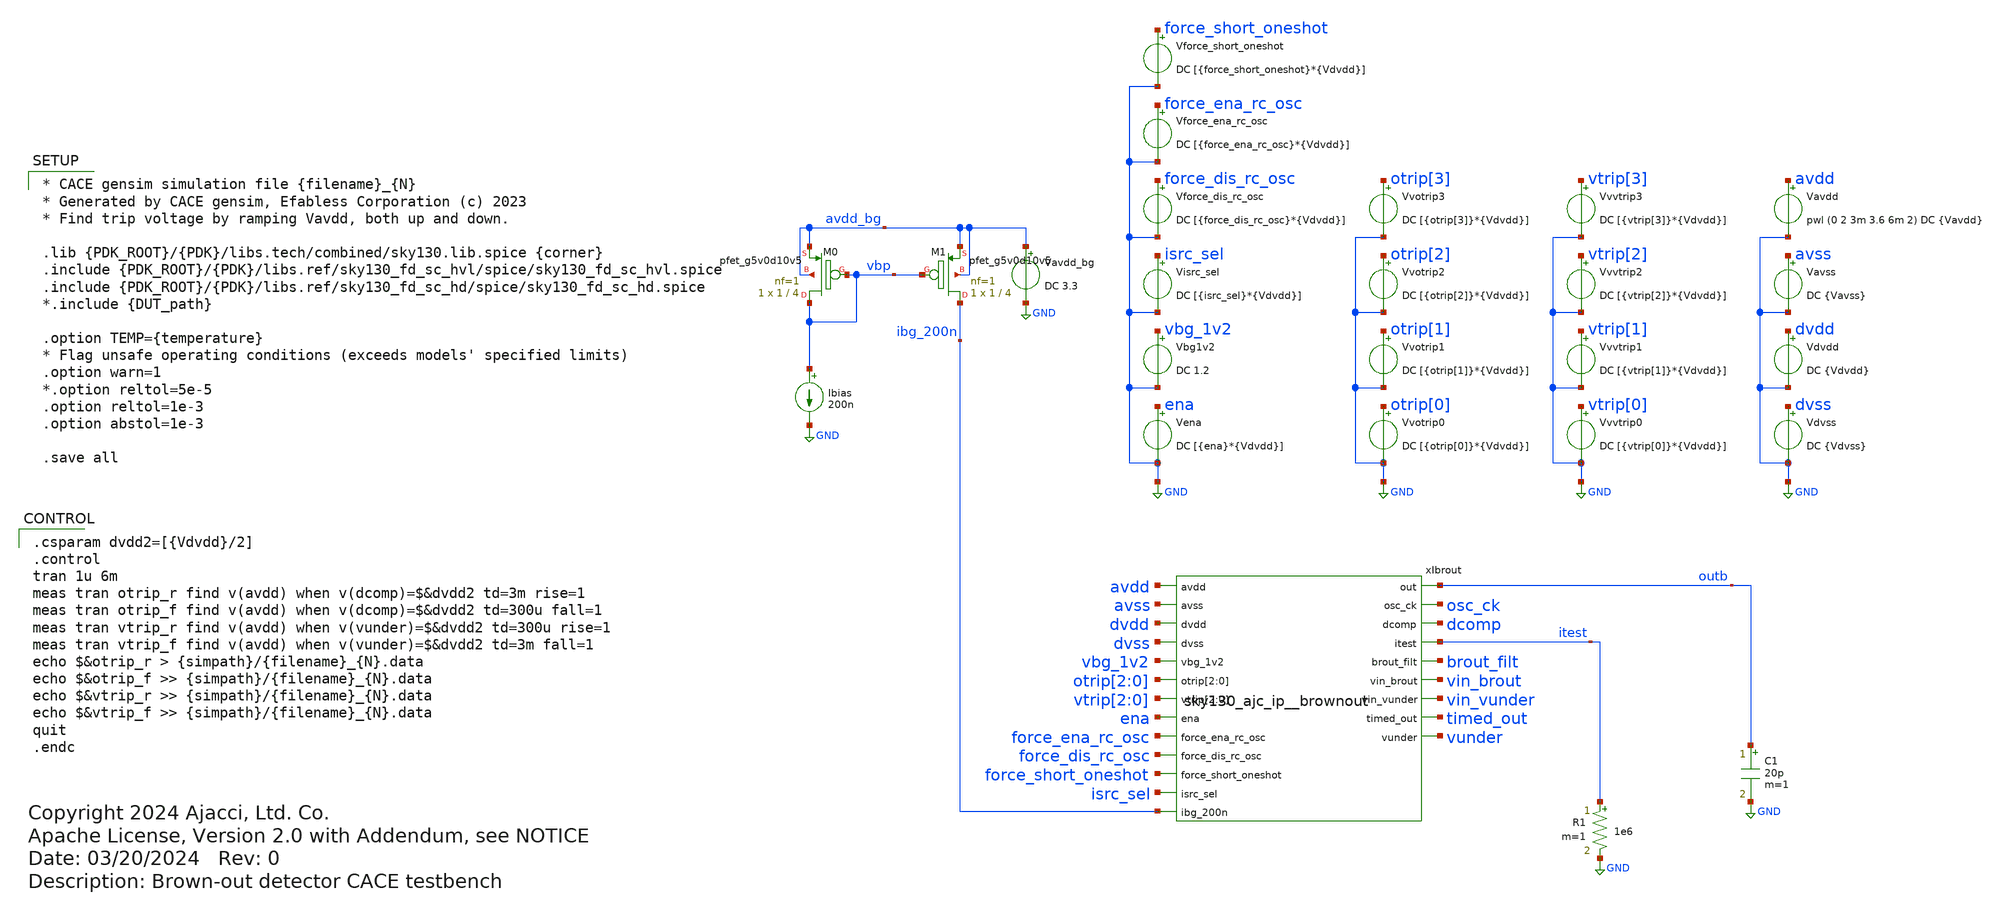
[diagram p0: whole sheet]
** sch_path: cace/trip_up_down.sch
* Copyright 2024 Ajacci, Ltd. Co.
* Apache License, Version 2.0 with Addendum, see NOTICE
**.subckt trip_up_down
Ibias vbp GND 200n
XM1 ibg_200n vbp avdd_bg avdd_bg sky130_fd_pr__pfet_g5v0d10v5 L=4 W=1 nf=1 ad='int((nf+1)/2) * W/nf * 0.29'
+ as='int((nf+2)/2) * W/nf * 0.29' pd='2*int((nf+1)/2) * (W/nf + 0.29)' ps='2*int((nf+2)/2) * (W/nf + 0.29)'
+ nrd='0.29 / W' nrs='0.29 / W' sa=0 sb=0 sd=0 mult=1 m=1
XM0 vbp vbp avdd_bg avdd_bg sky130_fd_pr__pfet_g5v0d10v5 L=4 W=1 nf=1 ad='int((nf+1)/2) * W/nf * 0.29'
+ as='int((nf+2)/2) * W/nf * 0.29' pd='2*int((nf+1)/2) * (W/nf + 0.29)' ps='2*int((nf+2)/2) * (W/nf + 0.29)'
+ nrd='0.29 / W' nrs='0.29 / W' sa=0 sb=0 sd=0 mult=1 m=1
R1 itest GND 1e6 m=1
C1 outb GND 20p m=1
xIbrout avdd avss outb dvdd osc_ck dvss dcomp vbg_1v2 otrip[2] otrip[1] otrip[0] itest brout_filt
+ vtrip[2] vtrip[1] vtrip[0] vin_brout ena force_ena_rc_osc vin_vunder force_dis_rc_osc timed_out vunder
+ force_short_oneshot isrc_sel ibg_200n sky130_ajc_ip__brownout
Vavss avss GND DC {Vavss}
Vena ena GND DC [{ena}*{Vdvdd}]
Vavdd avdd GND pwl (0 2 3m 3.6 6m 2) DC {Vavdd}
.save i(vavdd)
Vbg1v2 vbg_1v2 GND DC 1.2
Vdvss dvss GND DC {Vdvss}
Vdvdd dvdd GND DC {Vdvdd}
.save i(vdvdd)
Vvotrip0 otrip[0] GND DC [{otrip[0]}*{Vdvdd}]
.save i(vvotrip0)
Vvotrip1 otrip[1] GND DC [{otrip[1]}*{Vdvdd}]
.save i(vvotrip1)
Vvotrip2 otrip[2] GND DC [{otrip[2]}*{Vdvdd}]
.save i(vvotrip2)
Vvotrip3 otrip[3] GND DC [{otrip[3]}*{Vdvdd}]
.save i(vvotrip3)
Visrc_sel isrc_sel GND DC [{isrc_sel}*{Vdvdd}]
Vvvtrip0 vtrip[0] GND DC [{vtrip[0]}*{Vdvdd}]
.save i(vvvtrip0)
Vvvtrip1 vtrip[1] GND DC [{vtrip[1]}*{Vdvdd}]
.save i(vvvtrip1)
Vvvtrip2 vtrip[2] GND DC [{vtrip[2]}*{Vdvdd}]
.save i(vvvtrip2)
Vvvtrip3 vtrip[3] GND DC [{vtrip[3]}*{Vdvdd}]
.save i(vvvtrip3)
Vforce_dis_rc_osc force_dis_rc_osc GND DC [{force_dis_rc_osc}*{Vdvdd}]
Vforce_short_oneshot force_short_oneshot GND DC [{force_short_oneshot}*{Vdvdd}]
Vavdd_bg avdd_bg GND DC 3.3
Vforce_ena_rc_osc force_ena_rc_osc GND DC [{force_ena_rc_osc}*{Vdvdd}]
**** begin user architecture code

* CACE gensim simulation file {filename}_{N}
* Generated by CACE gensim, Efabless Corporation (c) 2023
* Find trip voltage by ramping Vavdd, both up and down.

.lib {PDK_ROOT}/{PDK}/libs.tech/combined/sky130.lib.spice {corner}
.include {PDK_ROOT}/{PDK}/libs.ref/sky130_fd_sc_hvl/spice/sky130_fd_sc_hvl.spice
.include {PDK_ROOT}/{PDK}/libs.ref/sky130_fd_sc_hd/spice/sky130_fd_sc_hd.spice
*.include {DUT_path}

.option TEMP={temperature}
* Flag unsafe operating conditions (exceeds models' specified limits)
.option warn=1
*.option reltol=5e-5
.option reltol=1e-3
.option abstol=1e-3

.save all



.csparam dvdd2=[{Vdvdd}/2]
.control
tran 1u 6m
meas tran otrip_r find v(avdd) when v(dcomp)=$&dvdd2 td=3m rise=1
meas tran otrip_f find v(avdd) when v(dcomp)=$&dvdd2 td=300u fall=1
meas tran vtrip_r find v(avdd) when v(vunder)=$&dvdd2 td=300u rise=1
meas tran vtrip_f find v(avdd) when v(vunder)=$&dvdd2 td=3m fall=1
echo $&otrip_r > {simpath}/{filename}_{N}.data
echo $&otrip_f >> {simpath}/{filename}_{N}.data
echo $&vtrip_r >> {simpath}/{filename}_{N}.data
echo $&vtrip_f >> {simpath}/{filename}_{N}.data
quit
.endc


**** end user architecture code
**.ends
.GLOBAL GND
.end
